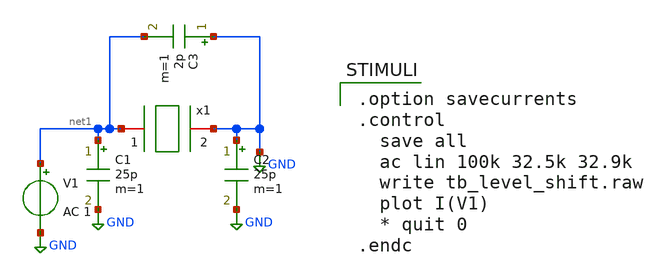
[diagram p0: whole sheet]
** sch_path: xschem/tb_xtal.sch
**.subckt tb_xtal
V1 net1 GND AC 1

x1 net1 GND xtal_iqd_125_1
C1 net1 GND 25p m=1
C2 GND GND 25p m=1
C3 GND net1 2p m=1
**** begin user architecture code

.option savecurrents
.control
  save all
  ac lin 100k 32.5k 32.9k
  write tb_level_shift.raw
  plot I(V1)
  * quit 0
.endc

**** end user architecture code
**.ends
.GLOBAL GND
.end
